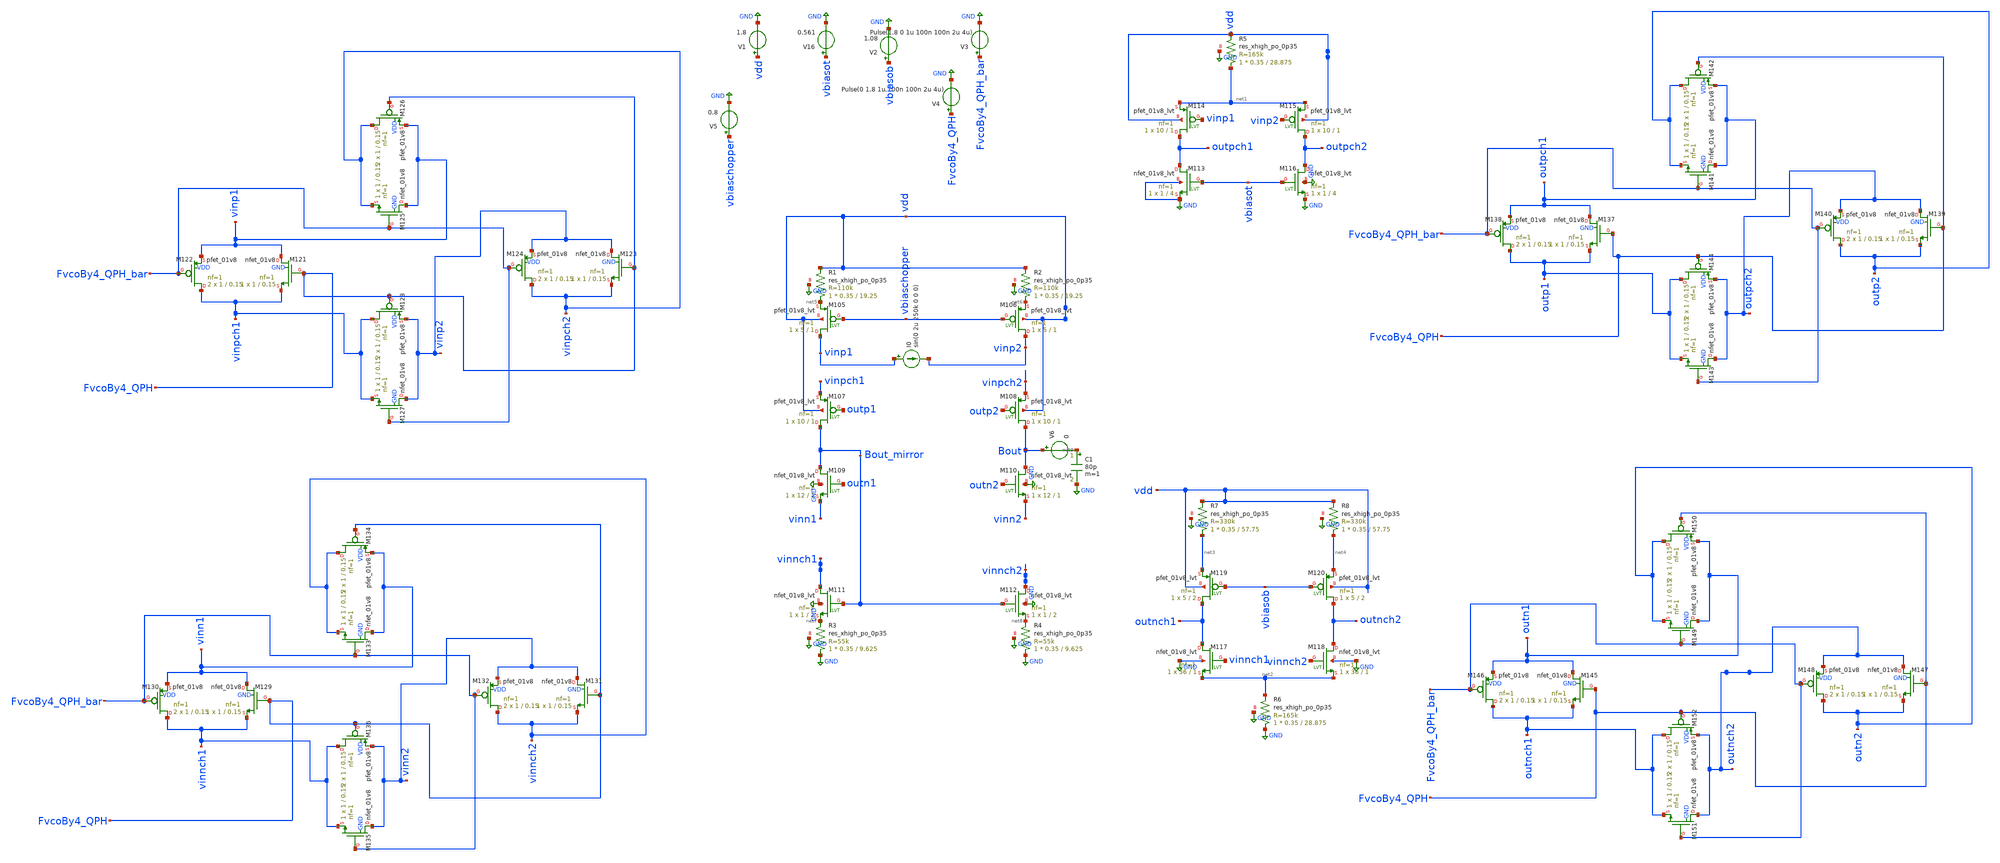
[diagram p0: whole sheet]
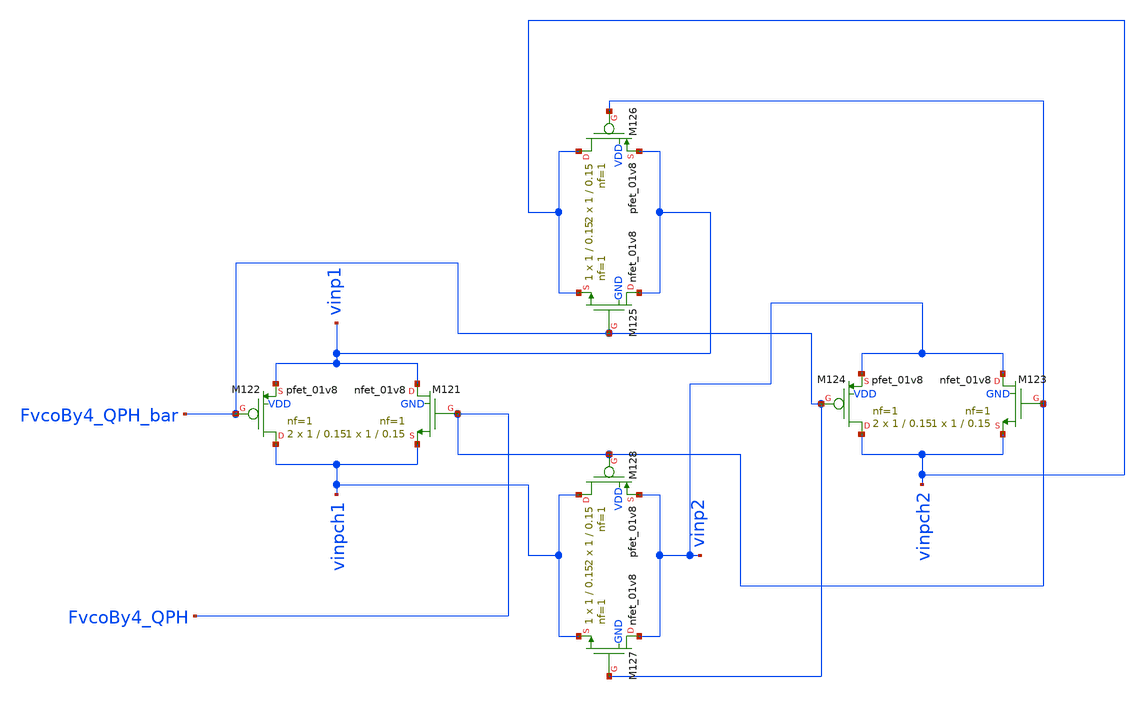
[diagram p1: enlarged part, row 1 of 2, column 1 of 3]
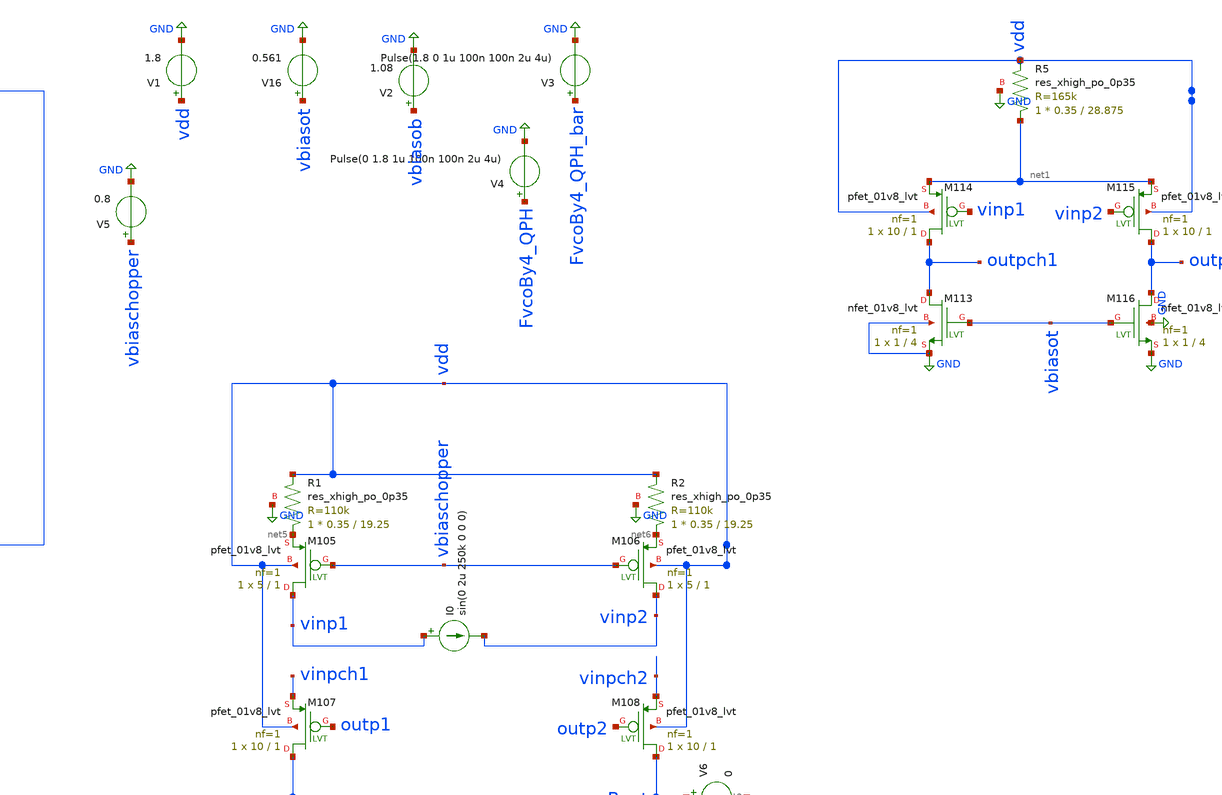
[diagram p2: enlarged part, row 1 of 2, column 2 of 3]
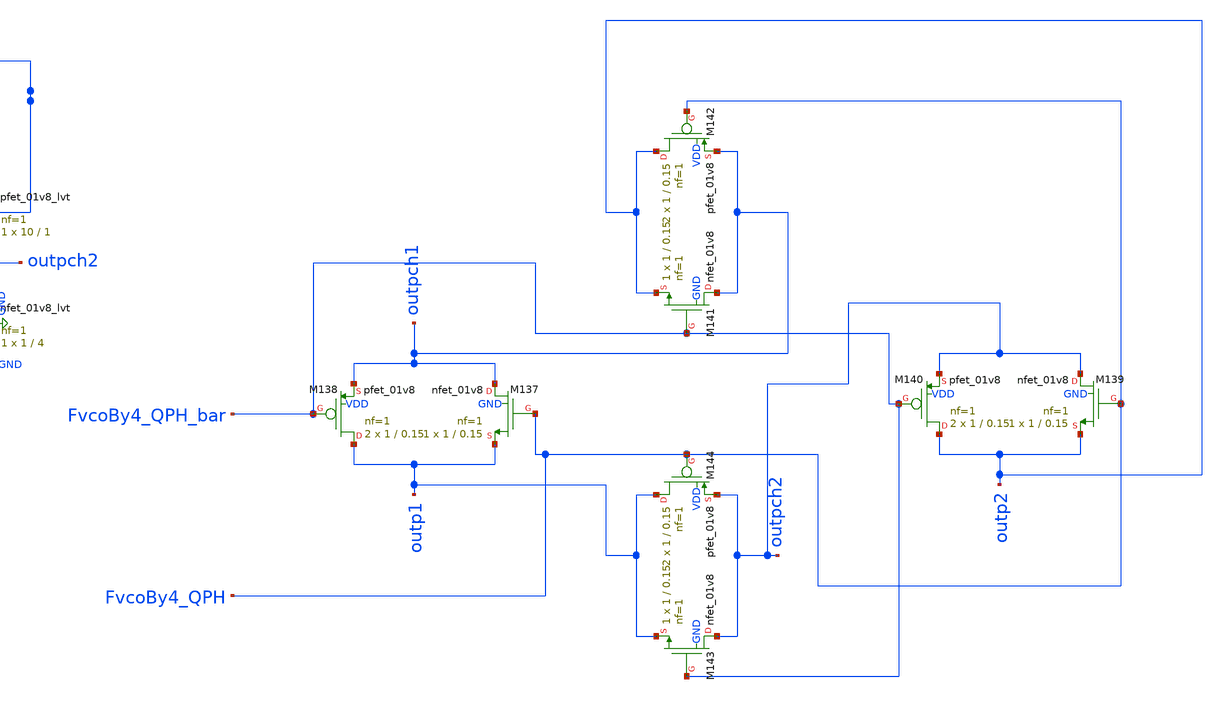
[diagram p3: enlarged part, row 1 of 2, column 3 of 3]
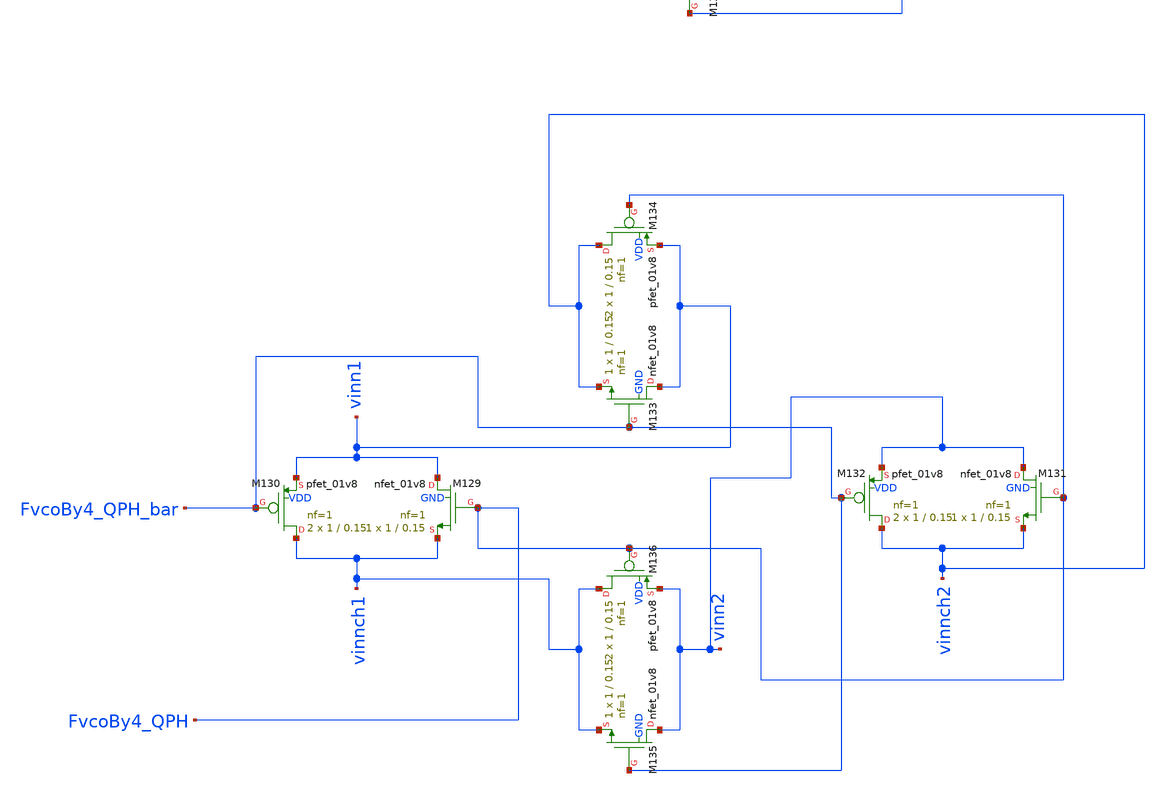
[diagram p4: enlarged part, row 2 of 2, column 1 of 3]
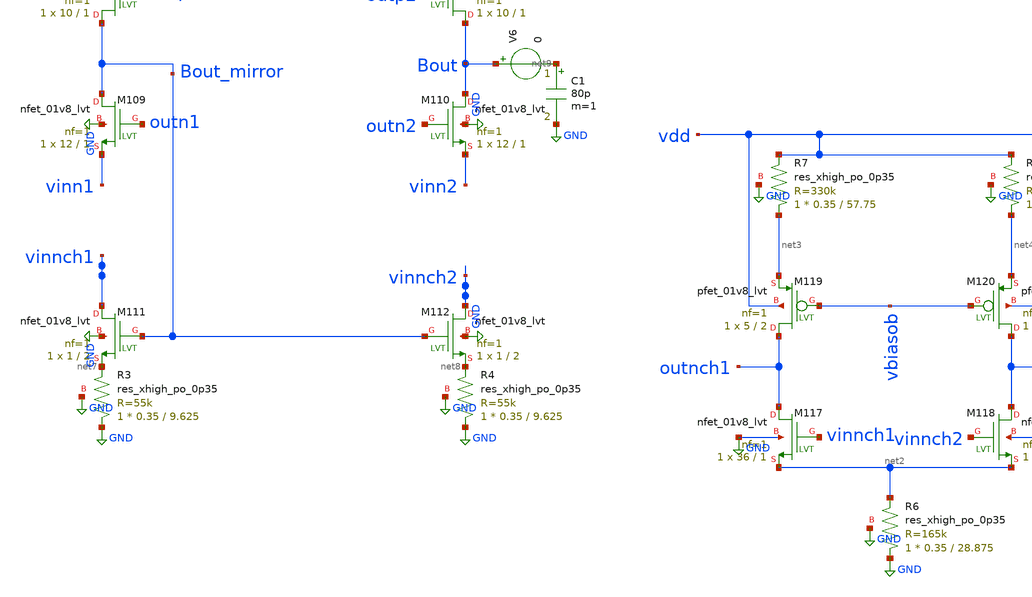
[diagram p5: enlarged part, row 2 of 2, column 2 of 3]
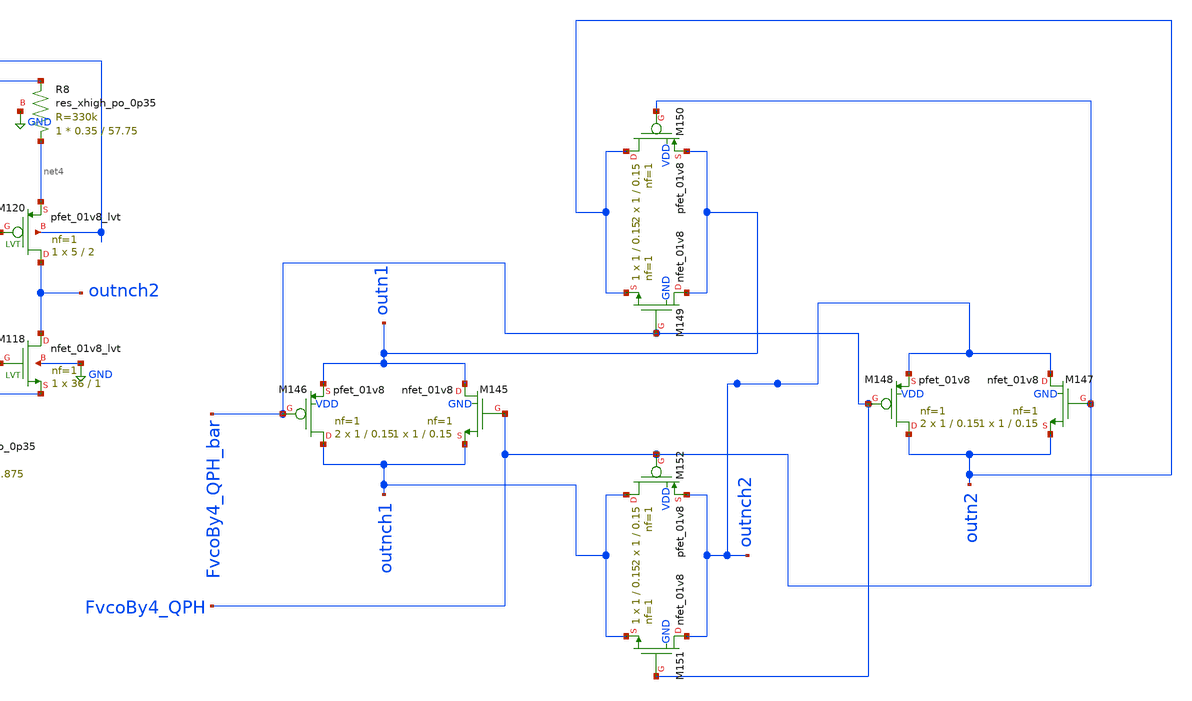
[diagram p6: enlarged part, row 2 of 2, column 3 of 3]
** sch_path: prelayout simulations/Wien Bridge/Cb and chopper/cb.sch
**.subckt cb
XM105 vinp1 vbiaschopper net5 vdd sky130_fd_pr__pfet_01v8_lvt L=1 W=5 nf=1 ad='int((nf+1)/2) * W/nf * 0.29'
+ as='int((nf+2)/2) * W/nf * 0.29' pd='2*int((nf+1)/2) * (W/nf + 0.29)' ps='2*int((nf+2)/2) * (W/nf + 0.29)'
+ nrd='0.29 / W' nrs='0.29 / W' sa=0 sb=0 sd=0 mult=1 m=1
XM106 vinp2 vbiaschopper net6 vdd sky130_fd_pr__pfet_01v8_lvt L=1 W=5 nf=1 ad='int((nf+1)/2) * W/nf * 0.29'
+ as='int((nf+2)/2) * W/nf * 0.29' pd='2*int((nf+1)/2) * (W/nf + 0.29)' ps='2*int((nf+2)/2) * (W/nf + 0.29)'
+ nrd='0.29 / W' nrs='0.29 / W' sa=0 sb=0 sd=0 mult=1 m=1
XM107 Bout_mirror outp1 vinpch1 vdd sky130_fd_pr__pfet_01v8_lvt L=1 W=10 nf=1 ad='int((nf+1)/2) * W/nf * 0.29'
+ as='int((nf+2)/2) * W/nf * 0.29' pd='2*int((nf+1)/2) * (W/nf + 0.29)' ps='2*int((nf+2)/2) * (W/nf + 0.29)'
+ nrd='0.29 / W' nrs='0.29 / W' sa=0 sb=0 sd=0 mult=1 m=1
XM108 Bout outp2 vinpch2 vdd sky130_fd_pr__pfet_01v8_lvt L=1 W=10 nf=1 ad='int((nf+1)/2) * W/nf * 0.29'
+ as='int((nf+2)/2) * W/nf * 0.29' pd='2*int((nf+1)/2) * (W/nf + 0.29)' ps='2*int((nf+2)/2) * (W/nf + 0.29)'
+ nrd='0.29 / W' nrs='0.29 / W' sa=0 sb=0 sd=0 mult=1 m=1
XM109 Bout_mirror outn1 vinn1 GND sky130_fd_pr__nfet_01v8_lvt L=1 W=12 nf=1 ad='int((nf+1)/2) * W/nf * 0.29'
+ as='int((nf+2)/2) * W/nf * 0.29' pd='2*int((nf+1)/2) * (W/nf + 0.29)' ps='2*int((nf+2)/2) * (W/nf + 0.29)'
+ nrd='0.29 / W' nrs='0.29 / W' sa=0 sb=0 sd=0 mult=1 m=1
XM110 Bout outn2 vinn2 GND sky130_fd_pr__nfet_01v8_lvt L=1 W=12 nf=1 ad='int((nf+1)/2) * W/nf * 0.29'
+ as='int((nf+2)/2) * W/nf * 0.29' pd='2*int((nf+1)/2) * (W/nf + 0.29)' ps='2*int((nf+2)/2) * (W/nf + 0.29)'
+ nrd='0.29 / W' nrs='0.29 / W' sa=0 sb=0 sd=0 mult=1 m=1
XM111 vinnch1 Bout_mirror net7 GND sky130_fd_pr__nfet_01v8_lvt L=2 W=1 nf=1 ad='int((nf+1)/2) * W/nf * 0.29'
+ as='int((nf+2)/2) * W/nf * 0.29' pd='2*int((nf+1)/2) * (W/nf + 0.29)' ps='2*int((nf+2)/2) * (W/nf + 0.29)'
+ nrd='0.29 / W' nrs='0.29 / W' sa=0 sb=0 sd=0 mult=1 m=1
XM112 vinnch2 Bout_mirror net8 GND sky130_fd_pr__nfet_01v8_lvt L=2 W=1 nf=1 ad='int((nf+1)/2) * W/nf * 0.29'
+ as='int((nf+2)/2) * W/nf * 0.29' pd='2*int((nf+1)/2) * (W/nf + 0.29)' ps='2*int((nf+2)/2) * (W/nf + 0.29)'
+ nrd='0.29 / W' nrs='0.29 / W' sa=0 sb=0 sd=0 mult=1 m=1
XM113 outpch1 vbiasot GND GND sky130_fd_pr__nfet_01v8_lvt L=4 W=1 nf=1 ad='int((nf+1)/2) * W/nf * 0.29'
+ as='int((nf+2)/2) * W/nf * 0.29' pd='2*int((nf+1)/2) * (W/nf + 0.29)' ps='2*int((nf+2)/2) * (W/nf + 0.29)'
+ nrd='0.29 / W' nrs='0.29 / W' sa=0 sb=0 sd=0 mult=1 m=1
XM114 outpch1 vinp1 net1 vdd sky130_fd_pr__pfet_01v8_lvt L=1 W=10 nf=1 ad='int((nf+1)/2) * W/nf * 0.29'
+ as='int((nf+2)/2) * W/nf * 0.29' pd='2*int((nf+1)/2) * (W/nf + 0.29)' ps='2*int((nf+2)/2) * (W/nf + 0.29)'
+ nrd='0.29 / W' nrs='0.29 / W' sa=0 sb=0 sd=0 mult=1 m=1
XM115 outpch2 vinp2 net1 vdd sky130_fd_pr__pfet_01v8_lvt L=1 W=10 nf=1 ad='int((nf+1)/2) * W/nf * 0.29'
+ as='int((nf+2)/2) * W/nf * 0.29' pd='2*int((nf+1)/2) * (W/nf + 0.29)' ps='2*int((nf+2)/2) * (W/nf + 0.29)'
+ nrd='0.29 / W' nrs='0.29 / W' sa=0 sb=0 sd=0 mult=1 m=1
XM116 outpch2 vbiasot GND GND sky130_fd_pr__nfet_01v8_lvt L=4 W=1 nf=1 ad='int((nf+1)/2) * W/nf * 0.29'
+ as='int((nf+2)/2) * W/nf * 0.29' pd='2*int((nf+1)/2) * (W/nf + 0.29)' ps='2*int((nf+2)/2) * (W/nf + 0.29)'
+ nrd='0.29 / W' nrs='0.29 / W' sa=0 sb=0 sd=0 mult=1 m=1
XM117 outnch1 vinnch1 net2 GND sky130_fd_pr__nfet_01v8_lvt L=1 W=36 nf=1 ad='int((nf+1)/2) * W/nf * 0.29'
+ as='int((nf+2)/2) * W/nf * 0.29' pd='2*int((nf+1)/2) * (W/nf + 0.29)' ps='2*int((nf+2)/2) * (W/nf + 0.29)'
+ nrd='0.29 / W' nrs='0.29 / W' sa=0 sb=0 sd=0 mult=1 m=1
XM118 outnch2 vinnch2 net2 GND sky130_fd_pr__nfet_01v8_lvt L=1 W=36 nf=1 ad='int((nf+1)/2) * W/nf * 0.29'
+ as='int((nf+2)/2) * W/nf * 0.29' pd='2*int((nf+1)/2) * (W/nf + 0.29)' ps='2*int((nf+2)/2) * (W/nf + 0.29)'
+ nrd='0.29 / W' nrs='0.29 / W' sa=0 sb=0 sd=0 mult=1 m=1
XM119 outnch1 vbiasob net3 vdd sky130_fd_pr__pfet_01v8_lvt L=2 W=5 nf=1 ad='int((nf+1)/2) * W/nf * 0.29'
+ as='int((nf+2)/2) * W/nf * 0.29' pd='2*int((nf+1)/2) * (W/nf + 0.29)' ps='2*int((nf+2)/2) * (W/nf + 0.29)'
+ nrd='0.29 / W' nrs='0.29 / W' sa=0 sb=0 sd=0 mult=1 m=1
XM120 outnch2 vbiasob net4 vdd sky130_fd_pr__pfet_01v8_lvt L=2 W=5 nf=1 ad='int((nf+1)/2) * W/nf * 0.29'
+ as='int((nf+2)/2) * W/nf * 0.29' pd='2*int((nf+1)/2) * (W/nf + 0.29)' ps='2*int((nf+2)/2) * (W/nf + 0.29)'
+ nrd='0.29 / W' nrs='0.29 / W' sa=0 sb=0 sd=0 mult=1 m=1
XM121 vinp1 FvcoBy4_QPH vinpch1 GND sky130_fd_pr__nfet_01v8 L=0.15 W=1 nf=1 ad='int((nf+1)/2) * W/nf * 0.29'
+ as='int((nf+2)/2) * W/nf * 0.29' pd='2*int((nf+1)/2) * (W/nf + 0.29)' ps='2*int((nf+2)/2) * (W/nf + 0.29)'
+ nrd='0.29 / W' nrs='0.29 / W' sa=0 sb=0 sd=0 mult=1 m=1
XM122 vinpch1 FvcoBy4_QPH_bar vinp1 VDD sky130_fd_pr__pfet_01v8 L=0.15 W=1 nf=1 ad='int((nf+1)/2) * W/nf * 0.29'
+ as='int((nf+2)/2) * W/nf * 0.29' pd='2*int((nf+1)/2) * (W/nf + 0.29)' ps='2*int((nf+2)/2) * (W/nf + 0.29)'
+ nrd='0.29 / W' nrs='0.29 / W' sa=0 sb=0 sd=0 mult=2 m=2
XM123 vinp2 FvcoBy4_QPH vinpch2 GND sky130_fd_pr__nfet_01v8 L=0.15 W=1 nf=1 ad='int((nf+1)/2) * W/nf * 0.29'
+ as='int((nf+2)/2) * W/nf * 0.29' pd='2*int((nf+1)/2) * (W/nf + 0.29)' ps='2*int((nf+2)/2) * (W/nf + 0.29)'
+ nrd='0.29 / W' nrs='0.29 / W' sa=0 sb=0 sd=0 mult=1 m=1
XM124 vinpch2 FvcoBy4_QPH_bar vinp2 VDD sky130_fd_pr__pfet_01v8 L=0.15 W=1 nf=1 ad='int((nf+1)/2) * W/nf * 0.29'
+ as='int((nf+2)/2) * W/nf * 0.29' pd='2*int((nf+1)/2) * (W/nf + 0.29)' ps='2*int((nf+2)/2) * (W/nf + 0.29)'
+ nrd='0.29 / W' nrs='0.29 / W' sa=0 sb=0 sd=0 mult=2 m=2
XM125 vinp1 FvcoBy4_QPH_bar vinpch2 GND sky130_fd_pr__nfet_01v8 L=0.15 W=1 nf=1 ad='int((nf+1)/2) * W/nf * 0.29'
+ as='int((nf+2)/2) * W/nf * 0.29' pd='2*int((nf+1)/2) * (W/nf + 0.29)' ps='2*int((nf+2)/2) * (W/nf + 0.29)'
+ nrd='0.29 / W' nrs='0.29 / W' sa=0 sb=0 sd=0 mult=1 m=1
XM126 vinpch2 FvcoBy4_QPH vinp1 VDD sky130_fd_pr__pfet_01v8 L=0.15 W=1 nf=1 ad='int((nf+1)/2) * W/nf * 0.29'
+ as='int((nf+2)/2) * W/nf * 0.29' pd='2*int((nf+1)/2) * (W/nf + 0.29)' ps='2*int((nf+2)/2) * (W/nf + 0.29)'
+ nrd='0.29 / W' nrs='0.29 / W' sa=0 sb=0 sd=0 mult=2 m=2
XM127 vinp2 FvcoBy4_QPH_bar vinpch1 GND sky130_fd_pr__nfet_01v8 L=0.15 W=1 nf=1 ad='int((nf+1)/2) * W/nf * 0.29'
+ as='int((nf+2)/2) * W/nf * 0.29' pd='2*int((nf+1)/2) * (W/nf + 0.29)' ps='2*int((nf+2)/2) * (W/nf + 0.29)'
+ nrd='0.29 / W' nrs='0.29 / W' sa=0 sb=0 sd=0 mult=1 m=1
XM128 vinpch1 FvcoBy4_QPH vinp2 VDD sky130_fd_pr__pfet_01v8 L=0.15 W=1 nf=1 ad='int((nf+1)/2) * W/nf * 0.29'
+ as='int((nf+2)/2) * W/nf * 0.29' pd='2*int((nf+1)/2) * (W/nf + 0.29)' ps='2*int((nf+2)/2) * (W/nf + 0.29)'
+ nrd='0.29 / W' nrs='0.29 / W' sa=0 sb=0 sd=0 mult=2 m=2
XM129 vinn1 FvcoBy4_QPH vinnch1 GND sky130_fd_pr__nfet_01v8 L=0.15 W=1 nf=1 ad='int((nf+1)/2) * W/nf * 0.29'
+ as='int((nf+2)/2) * W/nf * 0.29' pd='2*int((nf+1)/2) * (W/nf + 0.29)' ps='2*int((nf+2)/2) * (W/nf + 0.29)'
+ nrd='0.29 / W' nrs='0.29 / W' sa=0 sb=0 sd=0 mult=1 m=1
XM130 vinnch1 FvcoBy4_QPH_bar vinn1 VDD sky130_fd_pr__pfet_01v8 L=0.15 W=1 nf=1 ad='int((nf+1)/2) * W/nf * 0.29'
+ as='int((nf+2)/2) * W/nf * 0.29' pd='2*int((nf+1)/2) * (W/nf + 0.29)' ps='2*int((nf+2)/2) * (W/nf + 0.29)'
+ nrd='0.29 / W' nrs='0.29 / W' sa=0 sb=0 sd=0 mult=2 m=2
XM131 vinn2 FvcoBy4_QPH vinnch2 GND sky130_fd_pr__nfet_01v8 L=0.15 W=1 nf=1 ad='int((nf+1)/2) * W/nf * 0.29'
+ as='int((nf+2)/2) * W/nf * 0.29' pd='2*int((nf+1)/2) * (W/nf + 0.29)' ps='2*int((nf+2)/2) * (W/nf + 0.29)'
+ nrd='0.29 / W' nrs='0.29 / W' sa=0 sb=0 sd=0 mult=1 m=1
XM132 vinnch2 FvcoBy4_QPH_bar vinn2 VDD sky130_fd_pr__pfet_01v8 L=0.15 W=1 nf=1 ad='int((nf+1)/2) * W/nf * 0.29'
+ as='int((nf+2)/2) * W/nf * 0.29' pd='2*int((nf+1)/2) * (W/nf + 0.29)' ps='2*int((nf+2)/2) * (W/nf + 0.29)'
+ nrd='0.29 / W' nrs='0.29 / W' sa=0 sb=0 sd=0 mult=2 m=2
XM133 vinn1 FvcoBy4_QPH_bar vinnch2 GND sky130_fd_pr__nfet_01v8 L=0.15 W=1 nf=1 ad='int((nf+1)/2) * W/nf * 0.29'
+ as='int((nf+2)/2) * W/nf * 0.29' pd='2*int((nf+1)/2) * (W/nf + 0.29)' ps='2*int((nf+2)/2) * (W/nf + 0.29)'
+ nrd='0.29 / W' nrs='0.29 / W' sa=0 sb=0 sd=0 mult=1 m=1
XM134 vinnch2 FvcoBy4_QPH vinn1 VDD sky130_fd_pr__pfet_01v8 L=0.15 W=1 nf=1 ad='int((nf+1)/2) * W/nf * 0.29'
+ as='int((nf+2)/2) * W/nf * 0.29' pd='2*int((nf+1)/2) * (W/nf + 0.29)' ps='2*int((nf+2)/2) * (W/nf + 0.29)'
+ nrd='0.29 / W' nrs='0.29 / W' sa=0 sb=0 sd=0 mult=2 m=2
XM135 vinn2 FvcoBy4_QPH_bar vinnch1 GND sky130_fd_pr__nfet_01v8 L=0.15 W=1 nf=1 ad='int((nf+1)/2) * W/nf * 0.29'
+ as='int((nf+2)/2) * W/nf * 0.29' pd='2*int((nf+1)/2) * (W/nf + 0.29)' ps='2*int((nf+2)/2) * (W/nf + 0.29)'
+ nrd='0.29 / W' nrs='0.29 / W' sa=0 sb=0 sd=0 mult=1 m=1
XM136 vinnch1 FvcoBy4_QPH vinn2 VDD sky130_fd_pr__pfet_01v8 L=0.15 W=1 nf=1 ad='int((nf+1)/2) * W/nf * 0.29'
+ as='int((nf+2)/2) * W/nf * 0.29' pd='2*int((nf+1)/2) * (W/nf + 0.29)' ps='2*int((nf+2)/2) * (W/nf + 0.29)'
+ nrd='0.29 / W' nrs='0.29 / W' sa=0 sb=0 sd=0 mult=2 m=2
XM137 outpch1 FvcoBy4_QPH outp1 GND sky130_fd_pr__nfet_01v8 L=0.15 W=1 nf=1 ad='int((nf+1)/2) * W/nf * 0.29'
+ as='int((nf+2)/2) * W/nf * 0.29' pd='2*int((nf+1)/2) * (W/nf + 0.29)' ps='2*int((nf+2)/2) * (W/nf + 0.29)'
+ nrd='0.29 / W' nrs='0.29 / W' sa=0 sb=0 sd=0 mult=1 m=1
XM138 outp1 FvcoBy4_QPH_bar outpch1 VDD sky130_fd_pr__pfet_01v8 L=0.15 W=1 nf=1 ad='int((nf+1)/2) * W/nf * 0.29'
+ as='int((nf+2)/2) * W/nf * 0.29' pd='2*int((nf+1)/2) * (W/nf + 0.29)' ps='2*int((nf+2)/2) * (W/nf + 0.29)'
+ nrd='0.29 / W' nrs='0.29 / W' sa=0 sb=0 sd=0 mult=2 m=2
XM139 outpch2 FvcoBy4_QPH outp2 GND sky130_fd_pr__nfet_01v8 L=0.15 W=1 nf=1 ad='int((nf+1)/2) * W/nf * 0.29'
+ as='int((nf+2)/2) * W/nf * 0.29' pd='2*int((nf+1)/2) * (W/nf + 0.29)' ps='2*int((nf+2)/2) * (W/nf + 0.29)'
+ nrd='0.29 / W' nrs='0.29 / W' sa=0 sb=0 sd=0 mult=1 m=1
XM140 outp2 FvcoBy4_QPH_bar outpch2 VDD sky130_fd_pr__pfet_01v8 L=0.15 W=1 nf=1 ad='int((nf+1)/2) * W/nf * 0.29'
+ as='int((nf+2)/2) * W/nf * 0.29' pd='2*int((nf+1)/2) * (W/nf + 0.29)' ps='2*int((nf+2)/2) * (W/nf + 0.29)'
+ nrd='0.29 / W' nrs='0.29 / W' sa=0 sb=0 sd=0 mult=2 m=2
XM141 outpch1 FvcoBy4_QPH_bar outp2 GND sky130_fd_pr__nfet_01v8 L=0.15 W=1 nf=1 ad='int((nf+1)/2) * W/nf * 0.29'
+ as='int((nf+2)/2) * W/nf * 0.29' pd='2*int((nf+1)/2) * (W/nf + 0.29)' ps='2*int((nf+2)/2) * (W/nf + 0.29)'
+ nrd='0.29 / W' nrs='0.29 / W' sa=0 sb=0 sd=0 mult=1 m=1
XM142 outp2 FvcoBy4_QPH outpch1 VDD sky130_fd_pr__pfet_01v8 L=0.15 W=1 nf=1 ad='int((nf+1)/2) * W/nf * 0.29'
+ as='int((nf+2)/2) * W/nf * 0.29' pd='2*int((nf+1)/2) * (W/nf + 0.29)' ps='2*int((nf+2)/2) * (W/nf + 0.29)'
+ nrd='0.29 / W' nrs='0.29 / W' sa=0 sb=0 sd=0 mult=2 m=2
XM143 outpch2 FvcoBy4_QPH_bar outp1 GND sky130_fd_pr__nfet_01v8 L=0.15 W=1 nf=1 ad='int((nf+1)/2) * W/nf * 0.29'
+ as='int((nf+2)/2) * W/nf * 0.29' pd='2*int((nf+1)/2) * (W/nf + 0.29)' ps='2*int((nf+2)/2) * (W/nf + 0.29)'
+ nrd='0.29 / W' nrs='0.29 / W' sa=0 sb=0 sd=0 mult=1 m=1
XM144 outp1 FvcoBy4_QPH outpch2 VDD sky130_fd_pr__pfet_01v8 L=0.15 W=1 nf=1 ad='int((nf+1)/2) * W/nf * 0.29'
+ as='int((nf+2)/2) * W/nf * 0.29' pd='2*int((nf+1)/2) * (W/nf + 0.29)' ps='2*int((nf+2)/2) * (W/nf + 0.29)'
+ nrd='0.29 / W' nrs='0.29 / W' sa=0 sb=0 sd=0 mult=2 m=2
XM145 outn1 FvcoBy4_QPH outnch1 GND sky130_fd_pr__nfet_01v8 L=0.15 W=1 nf=1 ad='int((nf+1)/2) * W/nf * 0.29'
+ as='int((nf+2)/2) * W/nf * 0.29' pd='2*int((nf+1)/2) * (W/nf + 0.29)' ps='2*int((nf+2)/2) * (W/nf + 0.29)'
+ nrd='0.29 / W' nrs='0.29 / W' sa=0 sb=0 sd=0 mult=1 m=1
XM146 outnch1 FvcoBy4_QPH_bar outn1 VDD sky130_fd_pr__pfet_01v8 L=0.15 W=1 nf=1 ad='int((nf+1)/2) * W/nf * 0.29'
+ as='int((nf+2)/2) * W/nf * 0.29' pd='2*int((nf+1)/2) * (W/nf + 0.29)' ps='2*int((nf+2)/2) * (W/nf + 0.29)'
+ nrd='0.29 / W' nrs='0.29 / W' sa=0 sb=0 sd=0 mult=2 m=2
XM147 outnch2 FvcoBy4_QPH outn2 GND sky130_fd_pr__nfet_01v8 L=0.15 W=1 nf=1 ad='int((nf+1)/2) * W/nf * 0.29'
+ as='int((nf+2)/2) * W/nf * 0.29' pd='2*int((nf+1)/2) * (W/nf + 0.29)' ps='2*int((nf+2)/2) * (W/nf + 0.29)'
+ nrd='0.29 / W' nrs='0.29 / W' sa=0 sb=0 sd=0 mult=1 m=1
XM148 outn2 FvcoBy4_QPH_bar outnch2 VDD sky130_fd_pr__pfet_01v8 L=0.15 W=1 nf=1 ad='int((nf+1)/2) * W/nf * 0.29'
+ as='int((nf+2)/2) * W/nf * 0.29' pd='2*int((nf+1)/2) * (W/nf + 0.29)' ps='2*int((nf+2)/2) * (W/nf + 0.29)'
+ nrd='0.29 / W' nrs='0.29 / W' sa=0 sb=0 sd=0 mult=2 m=2
XM149 outn1 FvcoBy4_QPH_bar outn2 GND sky130_fd_pr__nfet_01v8 L=0.15 W=1 nf=1 ad='int((nf+1)/2) * W/nf * 0.29'
+ as='int((nf+2)/2) * W/nf * 0.29' pd='2*int((nf+1)/2) * (W/nf + 0.29)' ps='2*int((nf+2)/2) * (W/nf + 0.29)'
+ nrd='0.29 / W' nrs='0.29 / W' sa=0 sb=0 sd=0 mult=1 m=1
XM150 outn2 FvcoBy4_QPH outn1 VDD sky130_fd_pr__pfet_01v8 L=0.15 W=1 nf=1 ad='int((nf+1)/2) * W/nf * 0.29'
+ as='int((nf+2)/2) * W/nf * 0.29' pd='2*int((nf+1)/2) * (W/nf + 0.29)' ps='2*int((nf+2)/2) * (W/nf + 0.29)'
+ nrd='0.29 / W' nrs='0.29 / W' sa=0 sb=0 sd=0 mult=2 m=2
XM151 outnch2 FvcoBy4_QPH_bar outnch1 GND sky130_fd_pr__nfet_01v8 L=0.15 W=1 nf=1 ad='int((nf+1)/2) * W/nf * 0.29'
+ as='int((nf+2)/2) * W/nf * 0.29' pd='2*int((nf+1)/2) * (W/nf + 0.29)' ps='2*int((nf+2)/2) * (W/nf + 0.29)'
+ nrd='0.29 / W' nrs='0.29 / W' sa=0 sb=0 sd=0 mult=1 m=1
XM152 outnch1 FvcoBy4_QPH outnch2 VDD sky130_fd_pr__pfet_01v8 L=0.15 W=1 nf=1 ad='int((nf+1)/2) * W/nf * 0.29'
+ as='int((nf+2)/2) * W/nf * 0.29' pd='2*int((nf+1)/2) * (W/nf + 0.29)' ps='2*int((nf+2)/2) * (W/nf + 0.29)'
+ nrd='0.29 / W' nrs='0.29 / W' sa=0 sb=0 sd=0 mult=2 m=2
XR1 net5 vdd GND sky130_fd_pr__res_xhigh_po_0p35 L=19.25 mult=1 m=1
XR2 net6 vdd GND sky130_fd_pr__res_xhigh_po_0p35 L=19.25 mult=1 m=1
XR3 GND net7 GND sky130_fd_pr__res_xhigh_po_0p35 L=9.625 mult=1 m=1
XR4 GND net8 GND sky130_fd_pr__res_xhigh_po_0p35 L=9.625 mult=1 m=1
XR5 net1 vdd GND sky130_fd_pr__res_xhigh_po_0p35 L=28.875 mult=1 m=1
XR6 GND net2 GND sky130_fd_pr__res_xhigh_po_0p35 L=28.875 mult=1 m=1
XR7 net3 vdd GND sky130_fd_pr__res_xhigh_po_0p35 L=57.75 mult=1 m=1
XR8 net4 vdd GND sky130_fd_pr__res_xhigh_po_0p35 L=57.75 mult=1 m=1
V16 vbiasot GND 0.561
V1 vdd GND 1.8
V2 vbiasob GND 1.08
V3 FvcoBy4_QPH_bar GND Pulse(1.8 0 1u 100n 100n 2u 4u)
V4 FvcoBy4_QPH GND Pulse(0 1.8 1u 100n 100n 2u 4u)
V5 vbiaschopper GND 0.8
V6 Bout net9 0
C1 net9 GND 80p m=1
I0 vinp1 vinp2 sin(0 2u 250k 0 0 0)
**** begin user architecture code


.lib /home/cegrahul/open_pdks/sky130/sky130A/libs.tech/ngspice/sky130.lib.spice tt
.tran 1n 10u
.control
run
save all
set color0 = white
set color1 = black
plot i(v6)
.endc


**** end user architecture code
**.ends
.GLOBAL GND
.end
